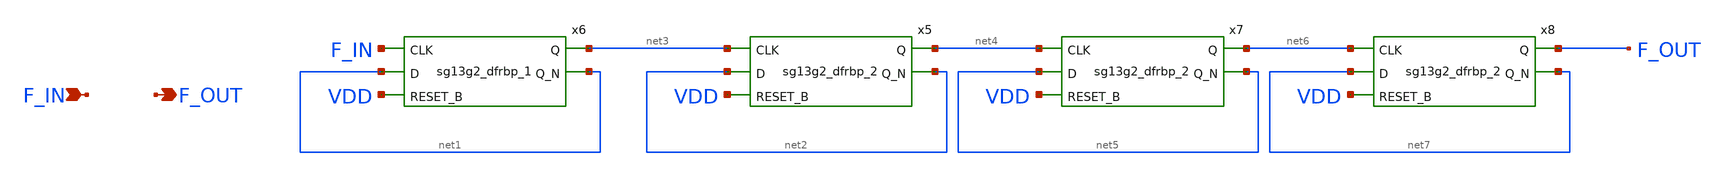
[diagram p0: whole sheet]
** sch_path: schematic/Test/FD/Freq_Div_std.sch
**.subckt Freq_Div_std F_OUT F_IN
*.opin F_OUT
*.ipin F_IN
x6 net3 net1 F_IN net1 VDD VDD GND sg13g2_dfrbp_1
x5 net4 net2 net3 net2 VDD VDD GND sg13g2_dfrbp_2
x7 net6 net5 net4 net5 VDD VDD GND sg13g2_dfrbp_2
x8 F_OUT net7 net6 net7 VDD VDD GND sg13g2_dfrbp_2
**.ends

* expanding   symbol:  sg13g2_stdcells/sg13g2_dfrbp_1.sym # of pins=5
** sym_path: sg13g2_stdcells/sg13g2_dfrbp_1.sym
** sch_path: sg13g2_stdcells/sg13g2_dfrbp_1.sch
.subckt sg13g2_dfrbp_1 Q Q_N CLK D RESET_B VDD VSS
*.ipin D
*.ipin RESET_B
*.ipin CLK
*.opin Q
*.opin Q_N
*.iopin VDD
*.iopin VSS
XM1 Db D net10 VSS sg13_lv_nmos w=420.00n l=130.00n ng=1 m=1 mm_ok=1
XM2 net10 RESET_B VSS VSS sg13_lv_nmos w=420.00n l=130.00n ng=1 m=1 mm_ok=1
XM3 net1 clkneg net9 VSS sg13_lv_nmos w=420.00n l=130.00n ng=1 m=1 mm_ok=1
XM4 net9 net1 VSS VSS sg13_lv_nmos w=420.00n l=130.00n ng=1 m=1 mm_ok=1
XM5 net1 net1 net5 VSS sg13_lv_nmos w=420.00n l=130.00n ng=1 m=1 mm_ok=1
XM6 net5 RESET_B VSS VSS sg13_lv_nmos w=420.00n l=130.00n ng=1 m=1 mm_ok=1
XM7 Q_N net1 VSS VSS sg13_lv_nmos w=740.00n l=130.00n ng=1 m=1 mm_ok=1
XM8 net2 net1 VSS VSS sg13_lv_nmos w=740.00n l=130.00n ng=1 m=1 mm_ok=1
XM9 Q net2 VSS VSS sg13_lv_nmos w=740.00n l=130.00n ng=1 m=1 mm_ok=1
XM10 clkneg CLK VSS VSS sg13_lv_nmos w=740.00n l=130.00n ng=1 m=1 mm_ok=1
XM11 clkpos clkneg VSS VSS sg13_lv_nmos w=740.00n l=130.00n ng=1 m=1 mm_ok=1
XM12 Db clkneg net3 VSS sg13_lv_nmos w=420.00n l=130.00n ng=1 m=1 mm_ok=1
XM13 net3 clkpos net8 VSS sg13_lv_nmos w=420.00n l=130.00n ng=1 m=1 mm_ok=1
XM14 net8 net3 net4 VSS sg13_lv_nmos w=420.00n l=130.00n ng=1 m=1 mm_ok=1
XM15 net4 RESET_B VSS VSS sg13_lv_nmos w=420.00n l=130.00n ng=1 m=1 mm_ok=1
XM16 net3 net3 VSS VSS sg13_lv_nmos w=740.00n l=130.00n ng=1 m=1 mm_ok=1
XM17 net3 clkpos net1 VSS sg13_lv_nmos w=740.00n l=130.00n ng=1 m=1 mm_ok=1
XM18 Db RESET_B VDD VDD sg13_lv_pmos w=420.00n l=130.00n ng=1 m=1 mm_ok=1
XM19 Db D VDD VDD sg13_lv_pmos w=420.00n l=130.00n ng=1 m=1 mm_ok=1
XM20 net7 net1 VDD VDD sg13_lv_pmos w=420.00n l=130.00n ng=1 m=1 mm_ok=1
XM21 net1 clkpos net7 VDD sg13_lv_pmos w=420.00n l=130.00n ng=1 m=1 mm_ok=1
XM22 net1 net1 VDD VDD sg13_lv_pmos w=420.00n l=130.00n ng=1 m=1 mm_ok=1
XM23 net1 RESET_B VDD VDD sg13_lv_pmos w=420.00n l=130.00n ng=1 m=1 mm_ok=1
XM24 Q_N net1 VDD VDD sg13_lv_pmos w=1.12u l=130.00n ng=1 m=1 mm_ok=1
XM25 net2 net1 VDD VDD sg13_lv_pmos w=1.12u l=130.00n ng=1 m=1 mm_ok=1
XM26 Q net2 VDD VDD sg13_lv_pmos w=1.12u l=130.00n ng=1 m=1 mm_ok=1
XM27 clkneg CLK VDD VDD sg13_lv_pmos w=1.12u l=130.00n ng=1 m=1 mm_ok=1
XM28 clkpos clkneg VDD VDD sg13_lv_pmos w=1.12u l=130.00n ng=1 m=1 mm_ok=1
XM29 Db clkpos net3 VDD sg13_lv_pmos w=420.00n l=130.00n ng=1 m=1 mm_ok=1
XM30 net6 net3 VDD VDD sg13_lv_pmos w=420.00n l=130.00n ng=1 m=1 mm_ok=1
XM31 net3 clkneg net6 VDD sg13_lv_pmos w=420.00n l=130.00n ng=1 m=1 mm_ok=1
XM32 net3 RESET_B VDD VDD sg13_lv_pmos w=420.00n l=130.00n ng=1 m=1 mm_ok=1
XM33 net3 net3 VDD VDD sg13_lv_pmos w=1.000u l=130.00n ng=1 m=1 mm_ok=1
XM34 net3 clkneg net1 VDD sg13_lv_pmos w=1.000u l=130.00n ng=1 m=1 mm_ok=1
.ends

.end
